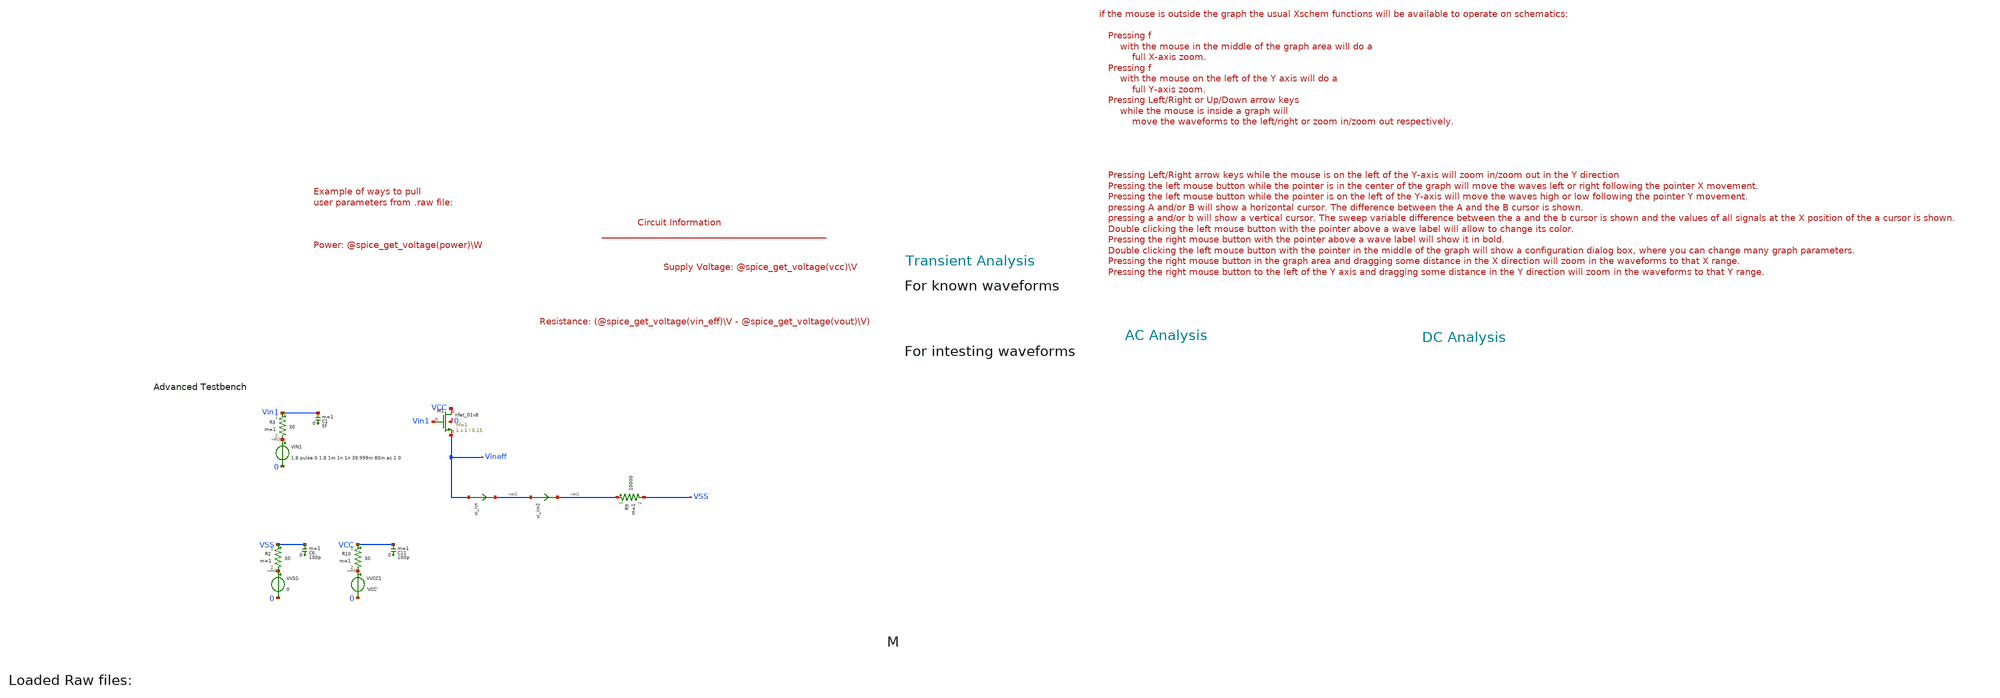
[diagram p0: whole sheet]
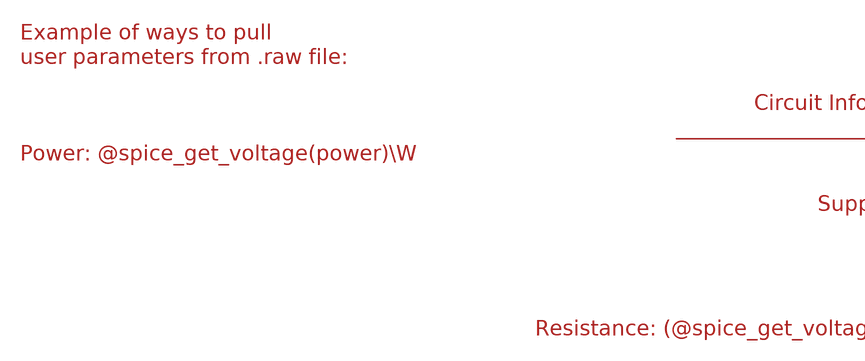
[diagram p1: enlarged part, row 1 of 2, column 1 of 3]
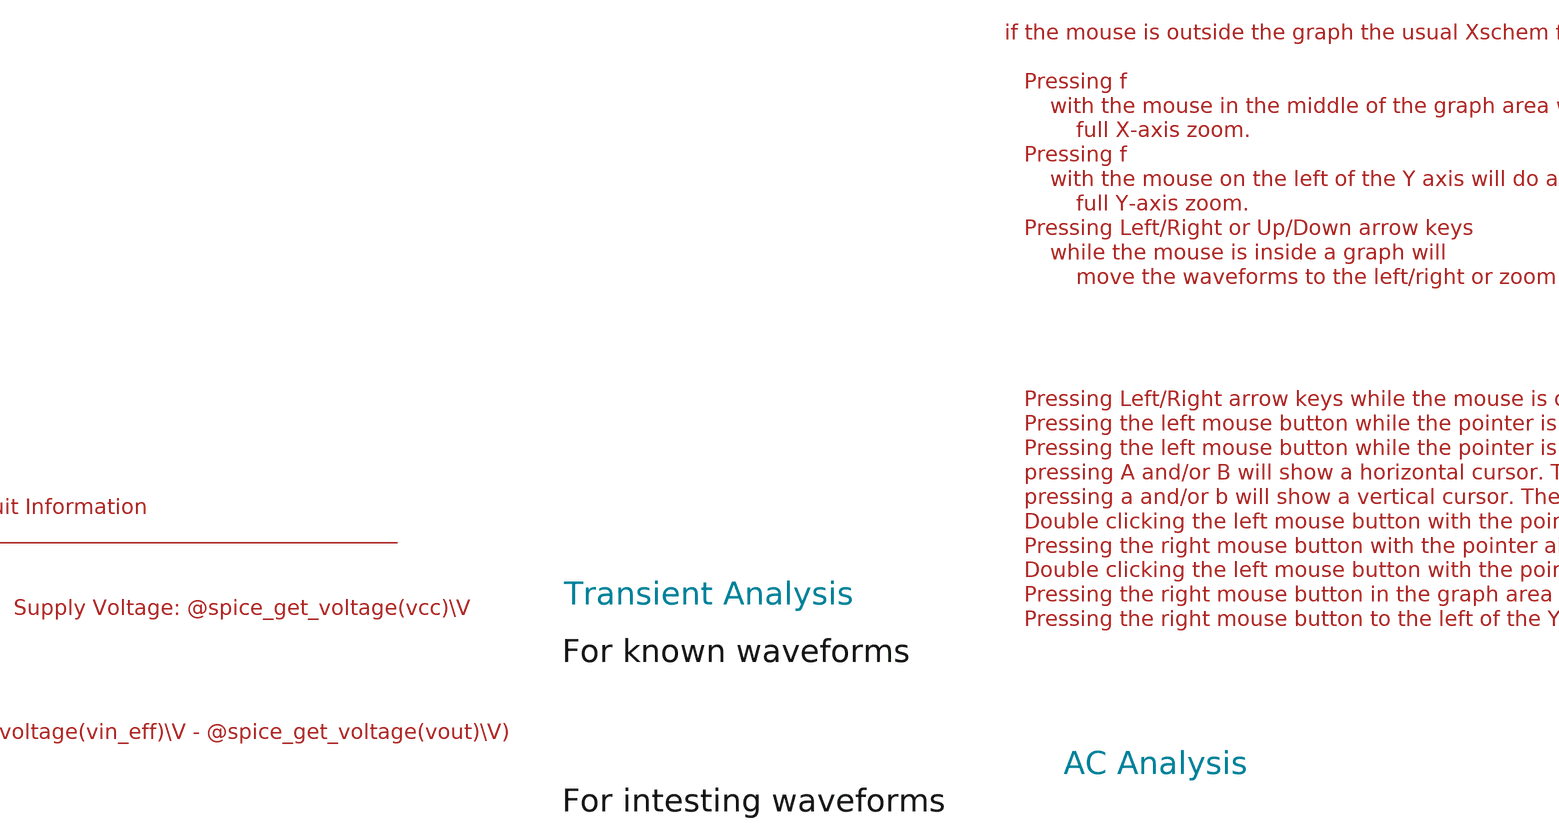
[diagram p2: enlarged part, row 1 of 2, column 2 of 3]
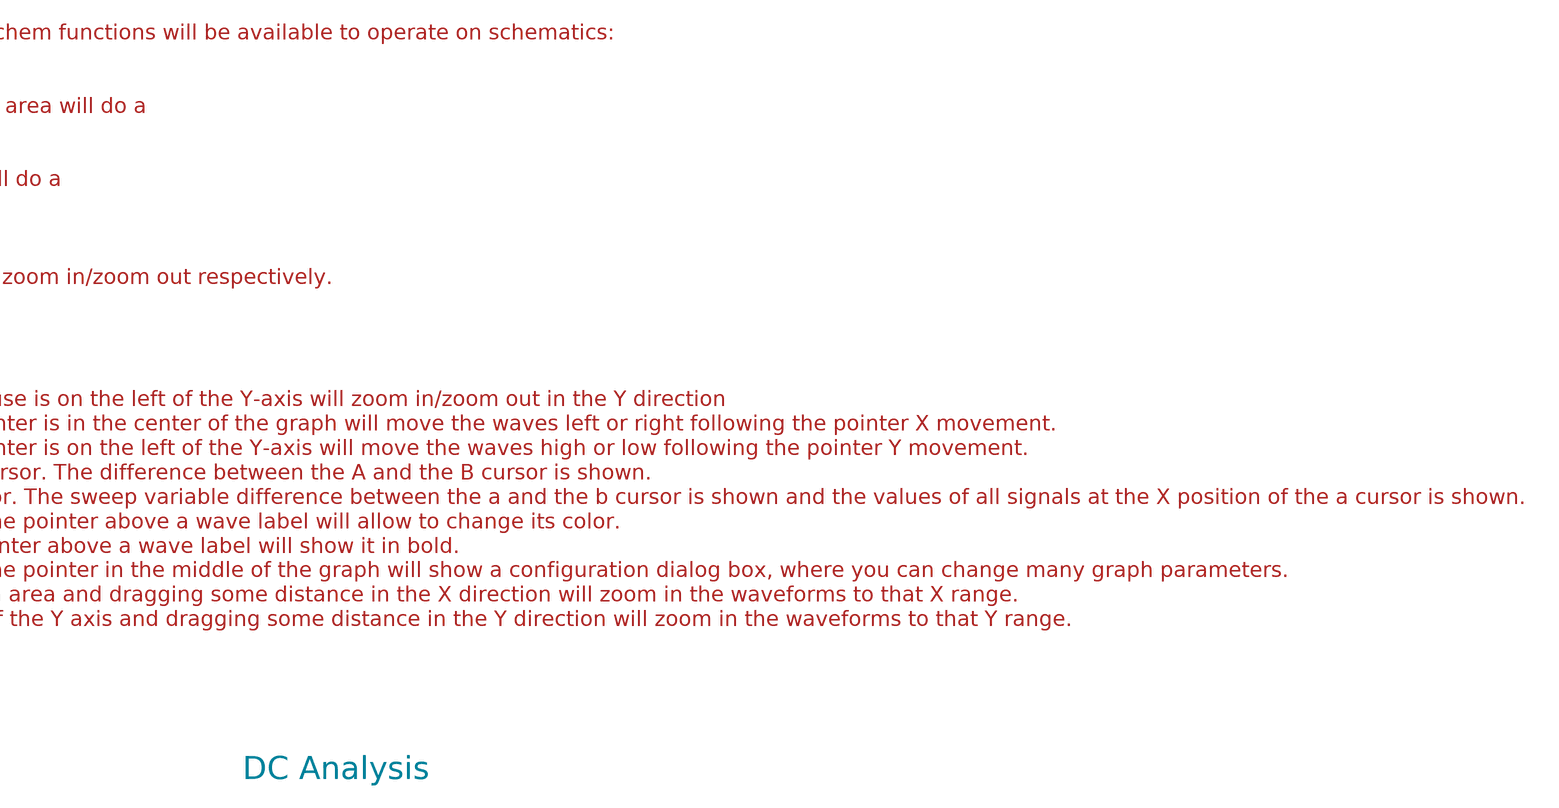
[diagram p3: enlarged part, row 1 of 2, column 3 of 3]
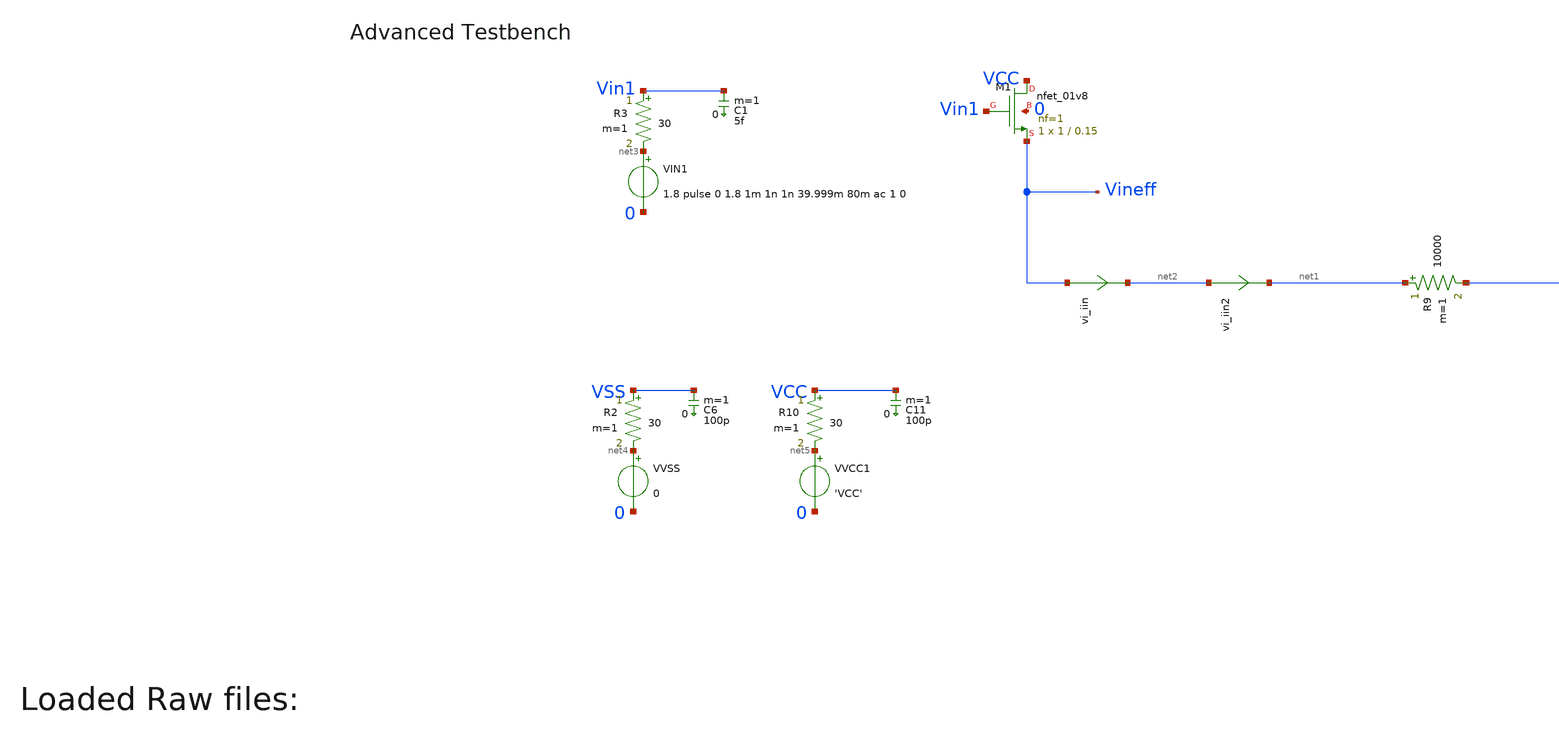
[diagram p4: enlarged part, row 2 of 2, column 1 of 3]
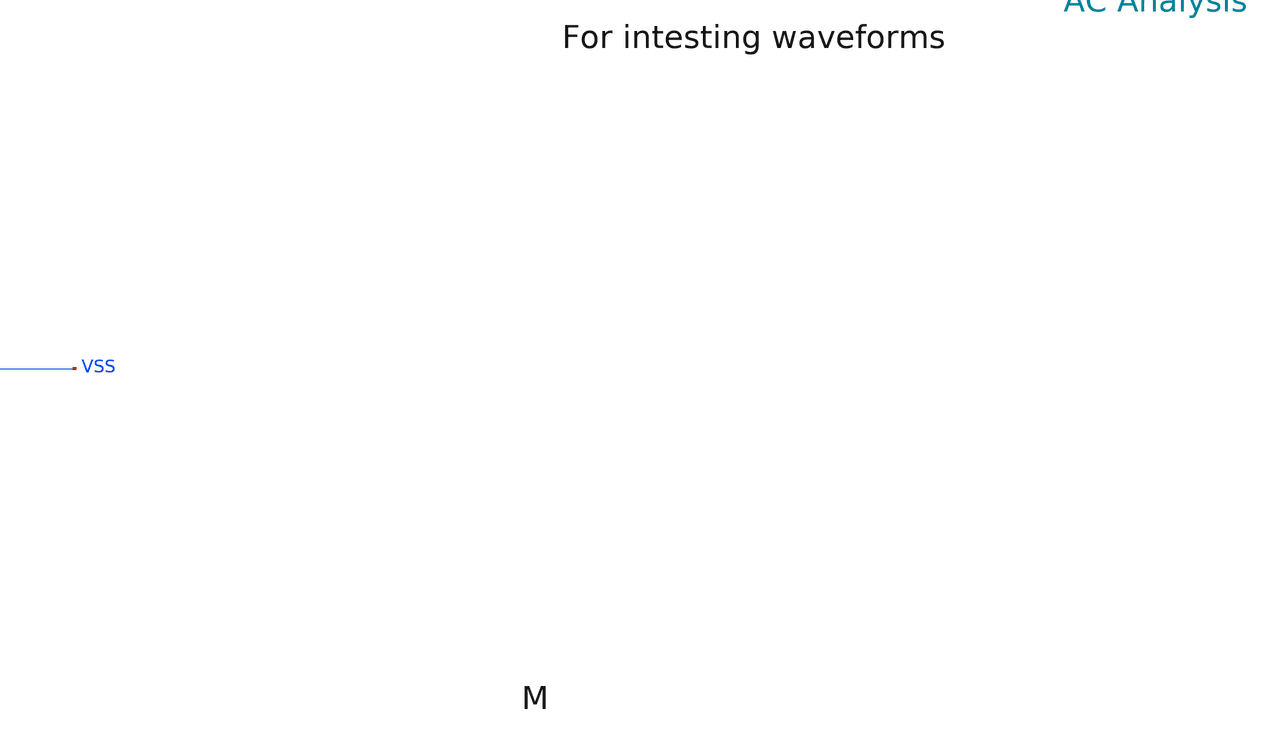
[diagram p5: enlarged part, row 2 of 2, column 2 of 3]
** sch_path: xschem/T0/RC/RC_tb.sch
* Copyright (C) 1998-2024 Stefan Frederik Schippers
* This program is free software; you can redistribute it and/or modify
* it under the terms of the GNU General Public License as published by
* the Free Software Foundation; either version 2 of the License, or
* (at your option) any later version.
* This program is distributed in the hope that it will be useful,
* but WITHOUT ANY WARRANTY; without even the implied warranty of
* MERCHANTABILITY or FITNESS FOR A PARTICULAR PURPOSE.  See the
* GNU General Public License for more details.
* You should have received a copy of the GNU General Public License
* along with this program; if not, write to the Free Software
**.subckt RC_tb
VIN1 net3 0 1.8 pulse 0 1.8 1m 1n 1n 39.999m 80m ac 1 0
R9 net1 VSS 10000 m=1
XM1 VCC Vin1 Vineff 0 sky130_fd_pr__nfet_01v8 L=0.15 W=1 nf=1 ad='int((1 + 1)/2) * 1 / 1 * 0.29' as='int((1 + 2)/2) * 1 / 1 * 0.29'
+ pd='2*int((1 + 1)/2) * (1 / 1 + 0.29)' ps='2*int((1 + 2)/2) * (1 / 1 + 0.29)' nrd='0.29 / 1 ' nrs='0.29 / 1 '
+ sa=0 sb=0 sd=0 mult=1 m=1
vi_iin Vineff net2 0
.save i(vi_iin)
vi_iin2 net2 net1 0
.save i(vi_iin2)
VVSS net4 0 0
R2 VSS net4 30 m=1
C6 VSS 0 100p m=1
VVCC1 net5 0 'VCC'
R10 VCC net5 30 m=1
C11 VCC 0 100p m=1
R3 Vin1 net3 30 m=1
C1 Vin1 0 5f m=1
**** begin user architecture code



.temp 30
*.param IB=1n
.param VCC = 1.8

.option savecurrents
.save all @m1[gm]
.control
  save all alli
  op
  let power=-v(vcc) * i(vvcc)
  settype power power
  write template_adv_tb.raw
  set appendwrite

  *dc vin1 0 1.8 0.001
  *write template_adv_tb.raw

  tran 1u 2m
  *tran 0.01n 15n
  write template_adv_tb.raw

  *ac dec 10 1 1G
  *remzerovec
  *write template_adv_tb.raw



  quit 0




.endc





** opencircuitdesign pdks install
.lib $::SKYWATER_MODELS/sky130.lib.spice tt


**** end user architecture code
**.ends
.end
